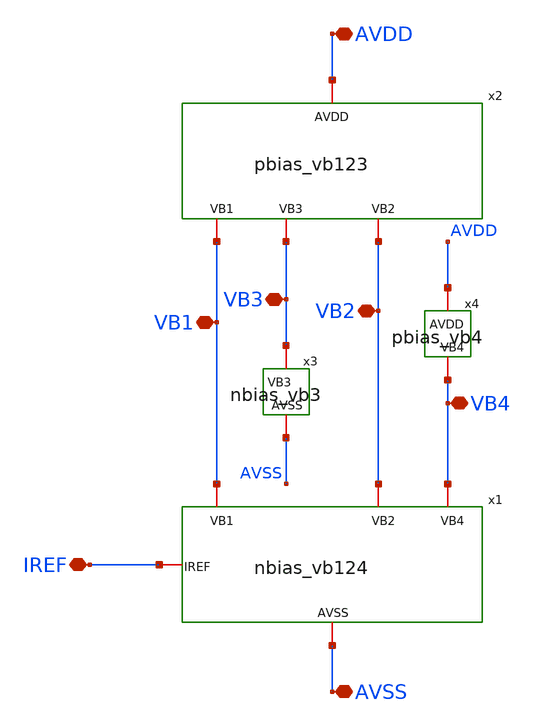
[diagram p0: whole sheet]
** sch_path: INA_layout_v2/bias/bias.sch
**.subckt bias IREF VB1 VB2 VB3 VB4 AVDD AVSS
*.iopin IREF
*.iopin VB1
*.iopin VB2
*.iopin VB3
*.iopin VB4
*.iopin AVDD
*.iopin AVSS
x1 IREF VB2 VB1 VB4 AVSS nbias_vb124
x2 VB3 VB1 VB2 AVDD pbias_vb123
x4 AVDD VB4 pbias_vb4
x3 VB3 AVSS nbias_vb3
**.ends

* expanding   symbol:  INA_layout_v2/bias/nbias_vb124.sym # of pins=5
** sym_path: INA_layout_v2/bias/nbias_vb124.sym
** sch_path: INA_layout_v2/bias/nbias_vb124.sch
.subckt nbias_vb124 IREF VB2 VB1 VB4 AVSS
*.iopin IREF
*.iopin VB1
*.iopin VB2
*.iopin VB4
*.iopin AVSS
x1[5] AVSS AVSS IREF IREF nfet_2series
x1[4] AVSS AVSS IREF IREF nfet_2series
x1[3] AVSS AVSS IREF IREF nfet_2series
x1[2] AVSS AVSS IREF IREF nfet_2series
x1[1] AVSS AVSS IREF IREF nfet_2series
x2[5] AVSS AVSS IREF VB1 nfet_2series
x2[4] AVSS AVSS IREF VB1 nfet_2series
x2[3] AVSS AVSS IREF VB1 nfet_2series
x2[2] AVSS AVSS IREF VB1 nfet_2series
x2[1] AVSS AVSS IREF VB1 nfet_2series
x3[5] AVSS AVSS VB2 VB2 nfet_2series
x3[4] AVSS AVSS VB2 VB2 nfet_2series
x3[3] AVSS AVSS VB2 VB2 nfet_2series
x3[2] AVSS AVSS VB2 VB2 nfet_2series
x3[1] AVSS AVSS VB2 VB2 nfet_2series
x4[5] AVSS AVSS VB2 VB4 nfet_2series
x4[4] AVSS AVSS VB2 VB4 nfet_2series
x4[3] AVSS AVSS VB2 VB4 nfet_2series
x4[2] AVSS AVSS VB2 VB4 nfet_2series
x4[1] AVSS AVSS VB2 VB4 nfet_2series
XM1 AVSS AVSS AVSS AVSS sky130_fd_pr__nfet_01v8 L=1 W=1 nf=1 ad='int((nf+1)/2) * W/nf * 0.29' as='int((nf+2)/2) * W/nf * 0.29'
+ pd='2*int((nf+1)/2) * (W/nf + 0.29)' ps='2*int((nf+2)/2) * (W/nf + 0.29)' nrd='0.29 / W' nrs='0.29 / W'
+ sa=0 sb=0 sd=0 mult=44 m=44
.ends


* expanding   symbol:  INA_layout_v2/bias/pbias_vb123.sym # of pins=4
** sym_path: INA_layout_v2/bias/pbias_vb123.sym
** sch_path: INA_layout_v2/bias/pbias_vb123.sch
.subckt pbias_vb123 VB3 VB1 VB2 AVDD
*.iopin VB1
*.iopin VB2
*.iopin VB3
*.iopin AVDD
x1[35] AVDD AVDD VB1 VB1 pfet_2series
x1[34] AVDD AVDD VB1 VB1 pfet_2series
x1[33] AVDD AVDD VB1 VB1 pfet_2series
x1[32] AVDD AVDD VB1 VB1 pfet_2series
x1[31] AVDD AVDD VB1 VB1 pfet_2series
x1[30] AVDD AVDD VB1 VB1 pfet_2series
x1[29] AVDD AVDD VB1 VB1 pfet_2series
x1[28] AVDD AVDD VB1 VB1 pfet_2series
x1[27] AVDD AVDD VB1 VB1 pfet_2series
x1[26] AVDD AVDD VB1 VB1 pfet_2series
x1[25] AVDD AVDD VB1 VB1 pfet_2series
x1[24] AVDD AVDD VB1 VB1 pfet_2series
x1[23] AVDD AVDD VB1 VB1 pfet_2series
x1[22] AVDD AVDD VB1 VB1 pfet_2series
x1[21] AVDD AVDD VB1 VB1 pfet_2series
x1[20] AVDD AVDD VB1 VB1 pfet_2series
x1[19] AVDD AVDD VB1 VB1 pfet_2series
x1[18] AVDD AVDD VB1 VB1 pfet_2series
x1[17] AVDD AVDD VB1 VB1 pfet_2series
x1[16] AVDD AVDD VB1 VB1 pfet_2series
x1[15] AVDD AVDD VB1 VB1 pfet_2series
x1[14] AVDD AVDD VB1 VB1 pfet_2series
x1[13] AVDD AVDD VB1 VB1 pfet_2series
x1[12] AVDD AVDD VB1 VB1 pfet_2series
x1[11] AVDD AVDD VB1 VB1 pfet_2series
x1[10] AVDD AVDD VB1 VB1 pfet_2series
x1[9] AVDD AVDD VB1 VB1 pfet_2series
x1[8] AVDD AVDD VB1 VB1 pfet_2series
x1[7] AVDD AVDD VB1 VB1 pfet_2series
x1[6] AVDD AVDD VB1 VB1 pfet_2series
x1[5] AVDD AVDD VB1 VB1 pfet_2series
x1[4] AVDD AVDD VB1 VB1 pfet_2series
x1[3] AVDD AVDD VB1 VB1 pfet_2series
x1[2] AVDD AVDD VB1 VB1 pfet_2series
x1[1] AVDD AVDD VB1 VB1 pfet_2series
x2[35] AVDD AVDD VB1 VB3 pfet_2series
x2[34] AVDD AVDD VB1 VB3 pfet_2series
x2[33] AVDD AVDD VB1 VB3 pfet_2series
x2[32] AVDD AVDD VB1 VB3 pfet_2series
x2[31] AVDD AVDD VB1 VB3 pfet_2series
x2[30] AVDD AVDD VB1 VB3 pfet_2series
x2[29] AVDD AVDD VB1 VB3 pfet_2series
x2[28] AVDD AVDD VB1 VB3 pfet_2series
x2[27] AVDD AVDD VB1 VB3 pfet_2series
x2[26] AVDD AVDD VB1 VB3 pfet_2series
x2[25] AVDD AVDD VB1 VB3 pfet_2series
x2[24] AVDD AVDD VB1 VB3 pfet_2series
x2[23] AVDD AVDD VB1 VB3 pfet_2series
x2[22] AVDD AVDD VB1 VB3 pfet_2series
x2[21] AVDD AVDD VB1 VB3 pfet_2series
x2[20] AVDD AVDD VB1 VB3 pfet_2series
x2[19] AVDD AVDD VB1 VB3 pfet_2series
x2[18] AVDD AVDD VB1 VB3 pfet_2series
x2[17] AVDD AVDD VB1 VB3 pfet_2series
x2[16] AVDD AVDD VB1 VB3 pfet_2series
x2[15] AVDD AVDD VB1 VB3 pfet_2series
x2[14] AVDD AVDD VB1 VB3 pfet_2series
x2[13] AVDD AVDD VB1 VB3 pfet_2series
x2[12] AVDD AVDD VB1 VB3 pfet_2series
x2[11] AVDD AVDD VB1 VB3 pfet_2series
x2[10] AVDD AVDD VB1 VB3 pfet_2series
x2[9] AVDD AVDD VB1 VB3 pfet_2series
x2[8] AVDD AVDD VB1 VB3 pfet_2series
x2[7] AVDD AVDD VB1 VB3 pfet_2series
x2[6] AVDD AVDD VB1 VB3 pfet_2series
x2[5] AVDD AVDD VB1 VB3 pfet_2series
x2[4] AVDD AVDD VB1 VB3 pfet_2series
x2[3] AVDD AVDD VB1 VB3 pfet_2series
x2[2] AVDD AVDD VB1 VB3 pfet_2series
x2[1] AVDD AVDD VB1 VB3 pfet_2series
x3[35] AVDD AVDD VB1 VB2 pfet_2series
x3[34] AVDD AVDD VB1 VB2 pfet_2series
x3[33] AVDD AVDD VB1 VB2 pfet_2series
x3[32] AVDD AVDD VB1 VB2 pfet_2series
x3[31] AVDD AVDD VB1 VB2 pfet_2series
x3[30] AVDD AVDD VB1 VB2 pfet_2series
x3[29] AVDD AVDD VB1 VB2 pfet_2series
x3[28] AVDD AVDD VB1 VB2 pfet_2series
x3[27] AVDD AVDD VB1 VB2 pfet_2series
x3[26] AVDD AVDD VB1 VB2 pfet_2series
x3[25] AVDD AVDD VB1 VB2 pfet_2series
x3[24] AVDD AVDD VB1 VB2 pfet_2series
x3[23] AVDD AVDD VB1 VB2 pfet_2series
x3[22] AVDD AVDD VB1 VB2 pfet_2series
x3[21] AVDD AVDD VB1 VB2 pfet_2series
x3[20] AVDD AVDD VB1 VB2 pfet_2series
x3[19] AVDD AVDD VB1 VB2 pfet_2series
x3[18] AVDD AVDD VB1 VB2 pfet_2series
x3[17] AVDD AVDD VB1 VB2 pfet_2series
x3[16] AVDD AVDD VB1 VB2 pfet_2series
x3[15] AVDD AVDD VB1 VB2 pfet_2series
x3[14] AVDD AVDD VB1 VB2 pfet_2series
x3[13] AVDD AVDD VB1 VB2 pfet_2series
x3[12] AVDD AVDD VB1 VB2 pfet_2series
x3[11] AVDD AVDD VB1 VB2 pfet_2series
x3[10] AVDD AVDD VB1 VB2 pfet_2series
x3[9] AVDD AVDD VB1 VB2 pfet_2series
x3[8] AVDD AVDD VB1 VB2 pfet_2series
x3[7] AVDD AVDD VB1 VB2 pfet_2series
x3[6] AVDD AVDD VB1 VB2 pfet_2series
x3[5] AVDD AVDD VB1 VB2 pfet_2series
x3[4] AVDD AVDD VB1 VB2 pfet_2series
x3[3] AVDD AVDD VB1 VB2 pfet_2series
x3[2] AVDD AVDD VB1 VB2 pfet_2series
x3[1] AVDD AVDD VB1 VB2 pfet_2series
XM1 AVDD AVDD AVDD AVDD sky130_fd_pr__pfet_01v8_hvt L=1 W=1 nf=1 ad='int((nf+1)/2) * W/nf * 0.29' as='int((nf+2)/2) * W/nf * 0.29'
+ pd='2*int((nf+1)/2) * (W/nf + 0.29)' ps='2*int((nf+2)/2) * (W/nf + 0.29)' nrd='0.29 / W' nrs='0.29 / W'
+ sa=0 sb=0 sd=0 mult=96 m=96
.ends


* expanding   symbol:  INA_layout_v2/bias/pbias_vb4.sym # of pins=2
** sym_path: INA_layout_v2/bias/pbias_vb4.sym
** sch_path: INA_layout_v2/bias/pbias_vb4.sch
.subckt pbias_vb4 AVDD VB4
*.iopin VB4
*.iopin AVDD
XM1 net1 VB4 AVDD AVDD sky130_fd_pr__pfet_01v8_hvt L=1 W=1 nf=1 ad='int((nf+1)/2) * W/nf * 0.29' as='int((nf+2)/2) * W/nf * 0.29'
+ pd='2*int((nf+1)/2) * (W/nf + 0.29)' ps='2*int((nf+2)/2) * (W/nf + 0.29)' nrd='0.29 / W' nrs='0.29 / W'
+ sa=0 sb=0 sd=0 mult=1 m=1
XM2 net2 VB4 net1 AVDD sky130_fd_pr__pfet_01v8_hvt L=1 W=1 nf=1 ad='int((nf+1)/2) * W/nf * 0.29' as='int((nf+2)/2) * W/nf * 0.29'
+ pd='2*int((nf+1)/2) * (W/nf + 0.29)' ps='2*int((nf+2)/2) * (W/nf + 0.29)' nrd='0.29 / W' nrs='0.29 / W'
+ sa=0 sb=0 sd=0 mult=1 m=1
XM3 VB4 VB4 net2 AVDD sky130_fd_pr__pfet_01v8_hvt L=1 W=1 nf=1 ad='int((nf+1)/2) * W/nf * 0.29' as='int((nf+2)/2) * W/nf * 0.29'
+ pd='2*int((nf+1)/2) * (W/nf + 0.29)' ps='2*int((nf+2)/2) * (W/nf + 0.29)' nrd='0.29 / W' nrs='0.29 / W'
+ sa=0 sb=0 sd=0 mult=1 m=1
XM4 net3 VB4 AVDD AVDD sky130_fd_pr__pfet_01v8_hvt L=1 W=1 nf=1 ad='int((nf+1)/2) * W/nf * 0.29' as='int((nf+2)/2) * W/nf * 0.29'
+ pd='2*int((nf+1)/2) * (W/nf + 0.29)' ps='2*int((nf+2)/2) * (W/nf + 0.29)' nrd='0.29 / W' nrs='0.29 / W'
+ sa=0 sb=0 sd=0 mult=1 m=1
XM5 net4 VB4 net3 AVDD sky130_fd_pr__pfet_01v8_hvt L=1 W=1 nf=1 ad='int((nf+1)/2) * W/nf * 0.29' as='int((nf+2)/2) * W/nf * 0.29'
+ pd='2*int((nf+1)/2) * (W/nf + 0.29)' ps='2*int((nf+2)/2) * (W/nf + 0.29)' nrd='0.29 / W' nrs='0.29 / W'
+ sa=0 sb=0 sd=0 mult=1 m=1
XM6 VB4 VB4 net4 AVDD sky130_fd_pr__pfet_01v8_hvt L=1 W=1 nf=1 ad='int((nf+1)/2) * W/nf * 0.29' as='int((nf+2)/2) * W/nf * 0.29'
+ pd='2*int((nf+1)/2) * (W/nf + 0.29)' ps='2*int((nf+2)/2) * (W/nf + 0.29)' nrd='0.29 / W' nrs='0.29 / W'
+ sa=0 sb=0 sd=0 mult=1 m=1
XM7 net5 VB4 AVDD AVDD sky130_fd_pr__pfet_01v8_hvt L=1 W=1 nf=1 ad='int((nf+1)/2) * W/nf * 0.29' as='int((nf+2)/2) * W/nf * 0.29'
+ pd='2*int((nf+1)/2) * (W/nf + 0.29)' ps='2*int((nf+2)/2) * (W/nf + 0.29)' nrd='0.29 / W' nrs='0.29 / W'
+ sa=0 sb=0 sd=0 mult=1 m=1
XM8 net6 VB4 net5 AVDD sky130_fd_pr__pfet_01v8_hvt L=1 W=1 nf=1 ad='int((nf+1)/2) * W/nf * 0.29' as='int((nf+2)/2) * W/nf * 0.29'
+ pd='2*int((nf+1)/2) * (W/nf + 0.29)' ps='2*int((nf+2)/2) * (W/nf + 0.29)' nrd='0.29 / W' nrs='0.29 / W'
+ sa=0 sb=0 sd=0 mult=1 m=1
XM9 VB4 VB4 net6 AVDD sky130_fd_pr__pfet_01v8_hvt L=1 W=1 nf=1 ad='int((nf+1)/2) * W/nf * 0.29' as='int((nf+2)/2) * W/nf * 0.29'
+ pd='2*int((nf+1)/2) * (W/nf + 0.29)' ps='2*int((nf+2)/2) * (W/nf + 0.29)' nrd='0.29 / W' nrs='0.29 / W'
+ sa=0 sb=0 sd=0 mult=1 m=1
XM10 net7 VB4 AVDD AVDD sky130_fd_pr__pfet_01v8_hvt L=1 W=1 nf=1 ad='int((nf+1)/2) * W/nf * 0.29' as='int((nf+2)/2) * W/nf * 0.29'
+ pd='2*int((nf+1)/2) * (W/nf + 0.29)' ps='2*int((nf+2)/2) * (W/nf + 0.29)' nrd='0.29 / W' nrs='0.29 / W'
+ sa=0 sb=0 sd=0 mult=1 m=1
XM11 net8 VB4 net7 AVDD sky130_fd_pr__pfet_01v8_hvt L=1 W=1 nf=1 ad='int((nf+1)/2) * W/nf * 0.29' as='int((nf+2)/2) * W/nf * 0.29'
+ pd='2*int((nf+1)/2) * (W/nf + 0.29)' ps='2*int((nf+2)/2) * (W/nf + 0.29)' nrd='0.29 / W' nrs='0.29 / W'
+ sa=0 sb=0 sd=0 mult=1 m=1
XM12 VB4 VB4 net8 AVDD sky130_fd_pr__pfet_01v8_hvt L=1 W=1 nf=1 ad='int((nf+1)/2) * W/nf * 0.29' as='int((nf+2)/2) * W/nf * 0.29'
+ pd='2*int((nf+1)/2) * (W/nf + 0.29)' ps='2*int((nf+2)/2) * (W/nf + 0.29)' nrd='0.29 / W' nrs='0.29 / W'
+ sa=0 sb=0 sd=0 mult=1 m=1
XM13 net9 VB4 AVDD AVDD sky130_fd_pr__pfet_01v8_hvt L=1 W=1 nf=1 ad='int((nf+1)/2) * W/nf * 0.29' as='int((nf+2)/2) * W/nf * 0.29'
+ pd='2*int((nf+1)/2) * (W/nf + 0.29)' ps='2*int((nf+2)/2) * (W/nf + 0.29)' nrd='0.29 / W' nrs='0.29 / W'
+ sa=0 sb=0 sd=0 mult=1 m=1
XM14 net10 VB4 net9 AVDD sky130_fd_pr__pfet_01v8_hvt L=1 W=1 nf=1 ad='int((nf+1)/2) * W/nf * 0.29' as='int((nf+2)/2) * W/nf * 0.29'
+ pd='2*int((nf+1)/2) * (W/nf + 0.29)' ps='2*int((nf+2)/2) * (W/nf + 0.29)' nrd='0.29 / W' nrs='0.29 / W'
+ sa=0 sb=0 sd=0 mult=1 m=1
XM15 VB4 VB4 net10 AVDD sky130_fd_pr__pfet_01v8_hvt L=1 W=1 nf=1 ad='int((nf+1)/2) * W/nf * 0.29' as='int((nf+2)/2) * W/nf * 0.29'
+ pd='2*int((nf+1)/2) * (W/nf + 0.29)' ps='2*int((nf+2)/2) * (W/nf + 0.29)' nrd='0.29 / W' nrs='0.29 / W'
+ sa=0 sb=0 sd=0 mult=1 m=1
XM16[20] AVDD AVDD AVDD AVDD sky130_fd_pr__pfet_01v8_hvt L=1 W=1 nf=1 ad='int((nf+1)/2) * W/nf * 0.29'
+ as='int((nf+2)/2) * W/nf * 0.29' pd='2*int((nf+1)/2) * (W/nf + 0.29)' ps='2*int((nf+2)/2) * (W/nf + 0.29)'
+ nrd='0.29 / W' nrs='0.29 / W' sa=0 sb=0 sd=0 mult=1 m=1
XM16[19] AVDD AVDD AVDD AVDD sky130_fd_pr__pfet_01v8_hvt L=1 W=1 nf=1 ad='int((nf+1)/2) * W/nf * 0.29'
+ as='int((nf+2)/2) * W/nf * 0.29' pd='2*int((nf+1)/2) * (W/nf + 0.29)' ps='2*int((nf+2)/2) * (W/nf + 0.29)'
+ nrd='0.29 / W' nrs='0.29 / W' sa=0 sb=0 sd=0 mult=1 m=1
XM16[18] AVDD AVDD AVDD AVDD sky130_fd_pr__pfet_01v8_hvt L=1 W=1 nf=1 ad='int((nf+1)/2) * W/nf * 0.29'
+ as='int((nf+2)/2) * W/nf * 0.29' pd='2*int((nf+1)/2) * (W/nf + 0.29)' ps='2*int((nf+2)/2) * (W/nf + 0.29)'
+ nrd='0.29 / W' nrs='0.29 / W' sa=0 sb=0 sd=0 mult=1 m=1
XM16[17] AVDD AVDD AVDD AVDD sky130_fd_pr__pfet_01v8_hvt L=1 W=1 nf=1 ad='int((nf+1)/2) * W/nf * 0.29'
+ as='int((nf+2)/2) * W/nf * 0.29' pd='2*int((nf+1)/2) * (W/nf + 0.29)' ps='2*int((nf+2)/2) * (W/nf + 0.29)'
+ nrd='0.29 / W' nrs='0.29 / W' sa=0 sb=0 sd=0 mult=1 m=1
XM16[16] AVDD AVDD AVDD AVDD sky130_fd_pr__pfet_01v8_hvt L=1 W=1 nf=1 ad='int((nf+1)/2) * W/nf * 0.29'
+ as='int((nf+2)/2) * W/nf * 0.29' pd='2*int((nf+1)/2) * (W/nf + 0.29)' ps='2*int((nf+2)/2) * (W/nf + 0.29)'
+ nrd='0.29 / W' nrs='0.29 / W' sa=0 sb=0 sd=0 mult=1 m=1
XM16[15] AVDD AVDD AVDD AVDD sky130_fd_pr__pfet_01v8_hvt L=1 W=1 nf=1 ad='int((nf+1)/2) * W/nf * 0.29'
+ as='int((nf+2)/2) * W/nf * 0.29' pd='2*int((nf+1)/2) * (W/nf + 0.29)' ps='2*int((nf+2)/2) * (W/nf + 0.29)'
+ nrd='0.29 / W' nrs='0.29 / W' sa=0 sb=0 sd=0 mult=1 m=1
XM16[14] AVDD AVDD AVDD AVDD sky130_fd_pr__pfet_01v8_hvt L=1 W=1 nf=1 ad='int((nf+1)/2) * W/nf * 0.29'
+ as='int((nf+2)/2) * W/nf * 0.29' pd='2*int((nf+1)/2) * (W/nf + 0.29)' ps='2*int((nf+2)/2) * (W/nf + 0.29)'
+ nrd='0.29 / W' nrs='0.29 / W' sa=0 sb=0 sd=0 mult=1 m=1
XM16[13] AVDD AVDD AVDD AVDD sky130_fd_pr__pfet_01v8_hvt L=1 W=1 nf=1 ad='int((nf+1)/2) * W/nf * 0.29'
+ as='int((nf+2)/2) * W/nf * 0.29' pd='2*int((nf+1)/2) * (W/nf + 0.29)' ps='2*int((nf+2)/2) * (W/nf + 0.29)'
+ nrd='0.29 / W' nrs='0.29 / W' sa=0 sb=0 sd=0 mult=1 m=1
XM16[12] AVDD AVDD AVDD AVDD sky130_fd_pr__pfet_01v8_hvt L=1 W=1 nf=1 ad='int((nf+1)/2) * W/nf * 0.29'
+ as='int((nf+2)/2) * W/nf * 0.29' pd='2*int((nf+1)/2) * (W/nf + 0.29)' ps='2*int((nf+2)/2) * (W/nf + 0.29)'
+ nrd='0.29 / W' nrs='0.29 / W' sa=0 sb=0 sd=0 mult=1 m=1
XM16[11] AVDD AVDD AVDD AVDD sky130_fd_pr__pfet_01v8_hvt L=1 W=1 nf=1 ad='int((nf+1)/2) * W/nf * 0.29'
+ as='int((nf+2)/2) * W/nf * 0.29' pd='2*int((nf+1)/2) * (W/nf + 0.29)' ps='2*int((nf+2)/2) * (W/nf + 0.29)'
+ nrd='0.29 / W' nrs='0.29 / W' sa=0 sb=0 sd=0 mult=1 m=1
XM16[10] AVDD AVDD AVDD AVDD sky130_fd_pr__pfet_01v8_hvt L=1 W=1 nf=1 ad='int((nf+1)/2) * W/nf * 0.29'
+ as='int((nf+2)/2) * W/nf * 0.29' pd='2*int((nf+1)/2) * (W/nf + 0.29)' ps='2*int((nf+2)/2) * (W/nf + 0.29)'
+ nrd='0.29 / W' nrs='0.29 / W' sa=0 sb=0 sd=0 mult=1 m=1
XM16[9] AVDD AVDD AVDD AVDD sky130_fd_pr__pfet_01v8_hvt L=1 W=1 nf=1 ad='int((nf+1)/2) * W/nf * 0.29'
+ as='int((nf+2)/2) * W/nf * 0.29' pd='2*int((nf+1)/2) * (W/nf + 0.29)' ps='2*int((nf+2)/2) * (W/nf + 0.29)'
+ nrd='0.29 / W' nrs='0.29 / W' sa=0 sb=0 sd=0 mult=1 m=1
XM16[8] AVDD AVDD AVDD AVDD sky130_fd_pr__pfet_01v8_hvt L=1 W=1 nf=1 ad='int((nf+1)/2) * W/nf * 0.29'
+ as='int((nf+2)/2) * W/nf * 0.29' pd='2*int((nf+1)/2) * (W/nf + 0.29)' ps='2*int((nf+2)/2) * (W/nf + 0.29)'
+ nrd='0.29 / W' nrs='0.29 / W' sa=0 sb=0 sd=0 mult=1 m=1
XM16[7] AVDD AVDD AVDD AVDD sky130_fd_pr__pfet_01v8_hvt L=1 W=1 nf=1 ad='int((nf+1)/2) * W/nf * 0.29'
+ as='int((nf+2)/2) * W/nf * 0.29' pd='2*int((nf+1)/2) * (W/nf + 0.29)' ps='2*int((nf+2)/2) * (W/nf + 0.29)'
+ nrd='0.29 / W' nrs='0.29 / W' sa=0 sb=0 sd=0 mult=1 m=1
XM16[6] AVDD AVDD AVDD AVDD sky130_fd_pr__pfet_01v8_hvt L=1 W=1 nf=1 ad='int((nf+1)/2) * W/nf * 0.29'
+ as='int((nf+2)/2) * W/nf * 0.29' pd='2*int((nf+1)/2) * (W/nf + 0.29)' ps='2*int((nf+2)/2) * (W/nf + 0.29)'
+ nrd='0.29 / W' nrs='0.29 / W' sa=0 sb=0 sd=0 mult=1 m=1
XM16[5] AVDD AVDD AVDD AVDD sky130_fd_pr__pfet_01v8_hvt L=1 W=1 nf=1 ad='int((nf+1)/2) * W/nf * 0.29'
+ as='int((nf+2)/2) * W/nf * 0.29' pd='2*int((nf+1)/2) * (W/nf + 0.29)' ps='2*int((nf+2)/2) * (W/nf + 0.29)'
+ nrd='0.29 / W' nrs='0.29 / W' sa=0 sb=0 sd=0 mult=1 m=1
XM16[4] AVDD AVDD AVDD AVDD sky130_fd_pr__pfet_01v8_hvt L=1 W=1 nf=1 ad='int((nf+1)/2) * W/nf * 0.29'
+ as='int((nf+2)/2) * W/nf * 0.29' pd='2*int((nf+1)/2) * (W/nf + 0.29)' ps='2*int((nf+2)/2) * (W/nf + 0.29)'
+ nrd='0.29 / W' nrs='0.29 / W' sa=0 sb=0 sd=0 mult=1 m=1
XM16[3] AVDD AVDD AVDD AVDD sky130_fd_pr__pfet_01v8_hvt L=1 W=1 nf=1 ad='int((nf+1)/2) * W/nf * 0.29'
+ as='int((nf+2)/2) * W/nf * 0.29' pd='2*int((nf+1)/2) * (W/nf + 0.29)' ps='2*int((nf+2)/2) * (W/nf + 0.29)'
+ nrd='0.29 / W' nrs='0.29 / W' sa=0 sb=0 sd=0 mult=1 m=1
XM16[2] AVDD AVDD AVDD AVDD sky130_fd_pr__pfet_01v8_hvt L=1 W=1 nf=1 ad='int((nf+1)/2) * W/nf * 0.29'
+ as='int((nf+2)/2) * W/nf * 0.29' pd='2*int((nf+1)/2) * (W/nf + 0.29)' ps='2*int((nf+2)/2) * (W/nf + 0.29)'
+ nrd='0.29 / W' nrs='0.29 / W' sa=0 sb=0 sd=0 mult=1 m=1
XM16[1] AVDD AVDD AVDD AVDD sky130_fd_pr__pfet_01v8_hvt L=1 W=1 nf=1 ad='int((nf+1)/2) * W/nf * 0.29'
+ as='int((nf+2)/2) * W/nf * 0.29' pd='2*int((nf+1)/2) * (W/nf + 0.29)' ps='2*int((nf+2)/2) * (W/nf + 0.29)'
+ nrd='0.29 / W' nrs='0.29 / W' sa=0 sb=0 sd=0 mult=1 m=1
.ends


* expanding   symbol:  INA_layout_v2/bias/nbias_vb3.sym # of pins=2
** sym_path: INA_layout_v2/bias/nbias_vb3.sym
** sch_path: INA_layout_v2/bias/nbias_vb3.sch
.subckt nbias_vb3 VB3 AVSS
*.iopin AVSS
*.iopin VB3
x1 AVSS AVSS VB3 net1 nfet_2series
x2 net1 AVSS VB3 VB3 nfet_2series
XM1[14] AVSS AVSS AVSS AVSS sky130_fd_pr__nfet_01v8 L=1 W=1 nf=1 ad='int((nf+1)/2) * W/nf * 0.29' as='int((nf+2)/2) * W/nf * 0.29'
+ pd='2*int((nf+1)/2) * (W/nf + 0.29)' ps='2*int((nf+2)/2) * (W/nf + 0.29)' nrd='0.29 / W' nrs='0.29 / W'
+ sa=0 sb=0 sd=0 mult=1 m=1
XM1[13] AVSS AVSS AVSS AVSS sky130_fd_pr__nfet_01v8 L=1 W=1 nf=1 ad='int((nf+1)/2) * W/nf * 0.29' as='int((nf+2)/2) * W/nf * 0.29'
+ pd='2*int((nf+1)/2) * (W/nf + 0.29)' ps='2*int((nf+2)/2) * (W/nf + 0.29)' nrd='0.29 / W' nrs='0.29 / W'
+ sa=0 sb=0 sd=0 mult=1 m=1
XM1[12] AVSS AVSS AVSS AVSS sky130_fd_pr__nfet_01v8 L=1 W=1 nf=1 ad='int((nf+1)/2) * W/nf * 0.29' as='int((nf+2)/2) * W/nf * 0.29'
+ pd='2*int((nf+1)/2) * (W/nf + 0.29)' ps='2*int((nf+2)/2) * (W/nf + 0.29)' nrd='0.29 / W' nrs='0.29 / W'
+ sa=0 sb=0 sd=0 mult=1 m=1
XM1[11] AVSS AVSS AVSS AVSS sky130_fd_pr__nfet_01v8 L=1 W=1 nf=1 ad='int((nf+1)/2) * W/nf * 0.29' as='int((nf+2)/2) * W/nf * 0.29'
+ pd='2*int((nf+1)/2) * (W/nf + 0.29)' ps='2*int((nf+2)/2) * (W/nf + 0.29)' nrd='0.29 / W' nrs='0.29 / W'
+ sa=0 sb=0 sd=0 mult=1 m=1
XM1[10] AVSS AVSS AVSS AVSS sky130_fd_pr__nfet_01v8 L=1 W=1 nf=1 ad='int((nf+1)/2) * W/nf * 0.29' as='int((nf+2)/2) * W/nf * 0.29'
+ pd='2*int((nf+1)/2) * (W/nf + 0.29)' ps='2*int((nf+2)/2) * (W/nf + 0.29)' nrd='0.29 / W' nrs='0.29 / W'
+ sa=0 sb=0 sd=0 mult=1 m=1
XM1[9] AVSS AVSS AVSS AVSS sky130_fd_pr__nfet_01v8 L=1 W=1 nf=1 ad='int((nf+1)/2) * W/nf * 0.29' as='int((nf+2)/2) * W/nf * 0.29'
+ pd='2*int((nf+1)/2) * (W/nf + 0.29)' ps='2*int((nf+2)/2) * (W/nf + 0.29)' nrd='0.29 / W' nrs='0.29 / W'
+ sa=0 sb=0 sd=0 mult=1 m=1
XM1[8] AVSS AVSS AVSS AVSS sky130_fd_pr__nfet_01v8 L=1 W=1 nf=1 ad='int((nf+1)/2) * W/nf * 0.29' as='int((nf+2)/2) * W/nf * 0.29'
+ pd='2*int((nf+1)/2) * (W/nf + 0.29)' ps='2*int((nf+2)/2) * (W/nf + 0.29)' nrd='0.29 / W' nrs='0.29 / W'
+ sa=0 sb=0 sd=0 mult=1 m=1
XM1[7] AVSS AVSS AVSS AVSS sky130_fd_pr__nfet_01v8 L=1 W=1 nf=1 ad='int((nf+1)/2) * W/nf * 0.29' as='int((nf+2)/2) * W/nf * 0.29'
+ pd='2*int((nf+1)/2) * (W/nf + 0.29)' ps='2*int((nf+2)/2) * (W/nf + 0.29)' nrd='0.29 / W' nrs='0.29 / W'
+ sa=0 sb=0 sd=0 mult=1 m=1
XM1[6] AVSS AVSS AVSS AVSS sky130_fd_pr__nfet_01v8 L=1 W=1 nf=1 ad='int((nf+1)/2) * W/nf * 0.29' as='int((nf+2)/2) * W/nf * 0.29'
+ pd='2*int((nf+1)/2) * (W/nf + 0.29)' ps='2*int((nf+2)/2) * (W/nf + 0.29)' nrd='0.29 / W' nrs='0.29 / W'
+ sa=0 sb=0 sd=0 mult=1 m=1
XM1[5] AVSS AVSS AVSS AVSS sky130_fd_pr__nfet_01v8 L=1 W=1 nf=1 ad='int((nf+1)/2) * W/nf * 0.29' as='int((nf+2)/2) * W/nf * 0.29'
+ pd='2*int((nf+1)/2) * (W/nf + 0.29)' ps='2*int((nf+2)/2) * (W/nf + 0.29)' nrd='0.29 / W' nrs='0.29 / W'
+ sa=0 sb=0 sd=0 mult=1 m=1
XM1[4] AVSS AVSS AVSS AVSS sky130_fd_pr__nfet_01v8 L=1 W=1 nf=1 ad='int((nf+1)/2) * W/nf * 0.29' as='int((nf+2)/2) * W/nf * 0.29'
+ pd='2*int((nf+1)/2) * (W/nf + 0.29)' ps='2*int((nf+2)/2) * (W/nf + 0.29)' nrd='0.29 / W' nrs='0.29 / W'
+ sa=0 sb=0 sd=0 mult=1 m=1
XM1[3] AVSS AVSS AVSS AVSS sky130_fd_pr__nfet_01v8 L=1 W=1 nf=1 ad='int((nf+1)/2) * W/nf * 0.29' as='int((nf+2)/2) * W/nf * 0.29'
+ pd='2*int((nf+1)/2) * (W/nf + 0.29)' ps='2*int((nf+2)/2) * (W/nf + 0.29)' nrd='0.29 / W' nrs='0.29 / W'
+ sa=0 sb=0 sd=0 mult=1 m=1
XM1[2] AVSS AVSS AVSS AVSS sky130_fd_pr__nfet_01v8 L=1 W=1 nf=1 ad='int((nf+1)/2) * W/nf * 0.29' as='int((nf+2)/2) * W/nf * 0.29'
+ pd='2*int((nf+1)/2) * (W/nf + 0.29)' ps='2*int((nf+2)/2) * (W/nf + 0.29)' nrd='0.29 / W' nrs='0.29 / W'
+ sa=0 sb=0 sd=0 mult=1 m=1
XM1[1] AVSS AVSS AVSS AVSS sky130_fd_pr__nfet_01v8 L=1 W=1 nf=1 ad='int((nf+1)/2) * W/nf * 0.29' as='int((nf+2)/2) * W/nf * 0.29'
+ pd='2*int((nf+1)/2) * (W/nf + 0.29)' ps='2*int((nf+2)/2) * (W/nf + 0.29)' nrd='0.29 / W' nrs='0.29 / W'
+ sa=0 sb=0 sd=0 mult=1 m=1
.ends


* expanding   symbol:  INA_layout_v2/bias/nfet_2series.sym # of pins=4
** sym_path: INA_layout_v2/bias/nfet_2series.sym
** sch_path: INA_layout_v2/bias/nfet_2series.sch
.subckt nfet_2series S B G D
*.iopin S
*.iopin B
*.iopin G
*.iopin D
XM1 D G net1 B sky130_fd_pr__nfet_01v8 L=1 W=1 nf=1 ad='int((nf+1)/2) * W/nf * 0.29' as='int((nf+2)/2) * W/nf * 0.29'
+ pd='2*int((nf+1)/2) * (W/nf + 0.29)' ps='2*int((nf+2)/2) * (W/nf + 0.29)' nrd='0.29 / W' nrs='0.29 / W'
+ sa=0 sb=0 sd=0 mult=1 m=1
XM2 net1 G S B sky130_fd_pr__nfet_01v8 L=1 W=1 nf=1 ad='int((nf+1)/2) * W/nf * 0.29' as='int((nf+2)/2) * W/nf * 0.29'
+ pd='2*int((nf+1)/2) * (W/nf + 0.29)' ps='2*int((nf+2)/2) * (W/nf + 0.29)' nrd='0.29 / W' nrs='0.29 / W'
+ sa=0 sb=0 sd=0 mult=1 m=1
.ends


* expanding   symbol:  INA_layout_v2/bias/pfet_2series.sym # of pins=4
** sym_path: INA_layout_v2/bias/pfet_2series.sym
** sch_path: INA_layout_v2/bias/pfet_2series.sch
.subckt pfet_2series S B G D
*.iopin S
*.iopin B
*.iopin G
*.iopin D
XM1 net1 G S B sky130_fd_pr__pfet_01v8_hvt L=1 W=1 nf=1 ad='int((nf+1)/2) * W/nf * 0.29' as='int((nf+2)/2) * W/nf * 0.29'
+ pd='2*int((nf+1)/2) * (W/nf + 0.29)' ps='2*int((nf+2)/2) * (W/nf + 0.29)' nrd='0.29 / W' nrs='0.29 / W'
+ sa=0 sb=0 sd=0 mult=1 m=1
XM2 D G net1 B sky130_fd_pr__pfet_01v8_hvt L=1 W=1 nf=1 ad='int((nf+1)/2) * W/nf * 0.29' as='int((nf+2)/2) * W/nf * 0.29'
+ pd='2*int((nf+1)/2) * (W/nf + 0.29)' ps='2*int((nf+2)/2) * (W/nf + 0.29)' nrd='0.29 / W' nrs='0.29 / W'
+ sa=0 sb=0 sd=0 mult=1 m=1
.ends

.end
